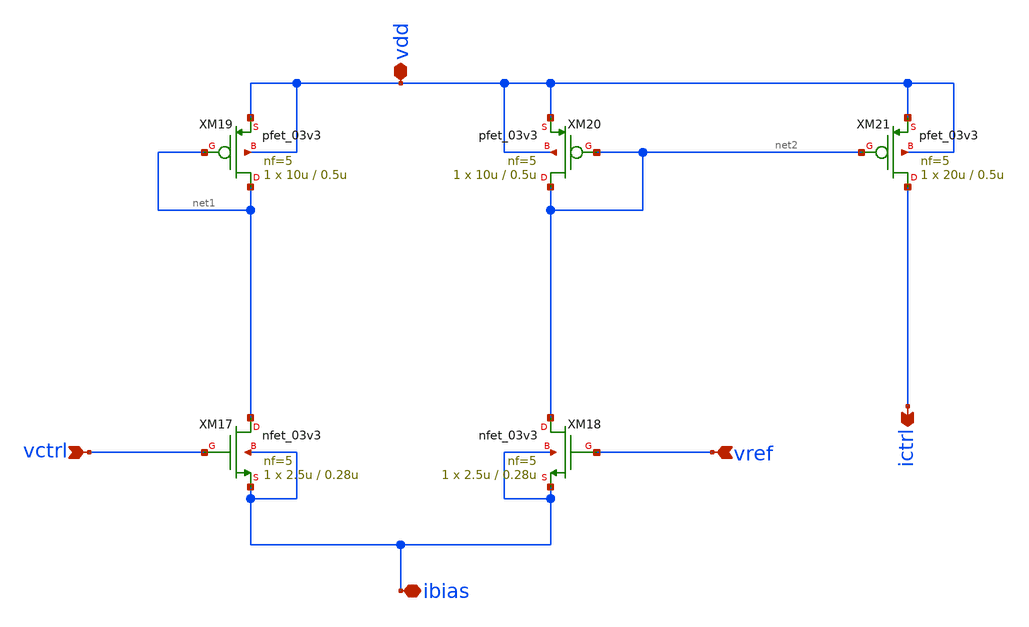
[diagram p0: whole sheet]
** sch_path: xschem/V2I.sch
**.subckt V2I vdd ibias vref vctrl ictrl
*.iopin vdd
*.iopin ibias
*.ipin vref
*.ipin vctrl
*.opin ictrl
XM17 net1 vctrl ibias ibias nfet_03v3 L=0.28u W=2.5u nf=5 ad='int((nf+1)/2) * W/nf * 0.18u' as='int((nf+2)/2) * W/nf * 0.18u'
+ pd='2*int((nf+1)/2) * (W/nf + 0.18u)' ps='2*int((nf+2)/2) * (W/nf + 0.18u)' nrd='0.18u / W' nrs='0.18u / W'
+ sa=0 sb=0 sd=0 m=1
XM18 net2 vref ibias ibias nfet_03v3 L=0.28u W=2.5u nf=5 ad='int((nf+1)/2) * W/nf * 0.18u' as='int((nf+2)/2) * W/nf * 0.18u'
+ pd='2*int((nf+1)/2) * (W/nf + 0.18u)' ps='2*int((nf+2)/2) * (W/nf + 0.18u)' nrd='0.18u / W' nrs='0.18u / W'
+ sa=0 sb=0 sd=0 m=1
XM19 net1 net1 vdd vdd pfet_03v3 L=0.5u W=10u nf=5 ad='int((nf+1)/2) * W/nf * 0.18u' as='int((nf+2)/2) * W/nf * 0.18u'
+ pd='2*int((nf+1)/2) * (W/nf + 0.18u)' ps='2*int((nf+2)/2) * (W/nf + 0.18u)' nrd='0.18u / W' nrs='0.18u / W'
+ sa=0 sb=0 sd=0 m=1
XM20 net2 net2 vdd vdd pfet_03v3 L=0.5u W=10u nf=5 ad='int((nf+1)/2) * W/nf * 0.18u' as='int((nf+2)/2) * W/nf * 0.18u'
+ pd='2*int((nf+1)/2) * (W/nf + 0.18u)' ps='2*int((nf+2)/2) * (W/nf + 0.18u)' nrd='0.18u / W' nrs='0.18u / W'
+ sa=0 sb=0 sd=0 m=1
XM21 ictrl net2 vdd vdd pfet_03v3 L=0.5u W=20u nf=5 ad='int((nf+1)/2) * W/nf * 0.18u' as='int((nf+2)/2) * W/nf * 0.18u'
+ pd='2*int((nf+1)/2) * (W/nf + 0.18u)' ps='2*int((nf+2)/2) * (W/nf + 0.18u)' nrd='0.18u / W' nrs='0.18u / W'
+ sa=0 sb=0 sd=0 m=1
**.ends
.end
